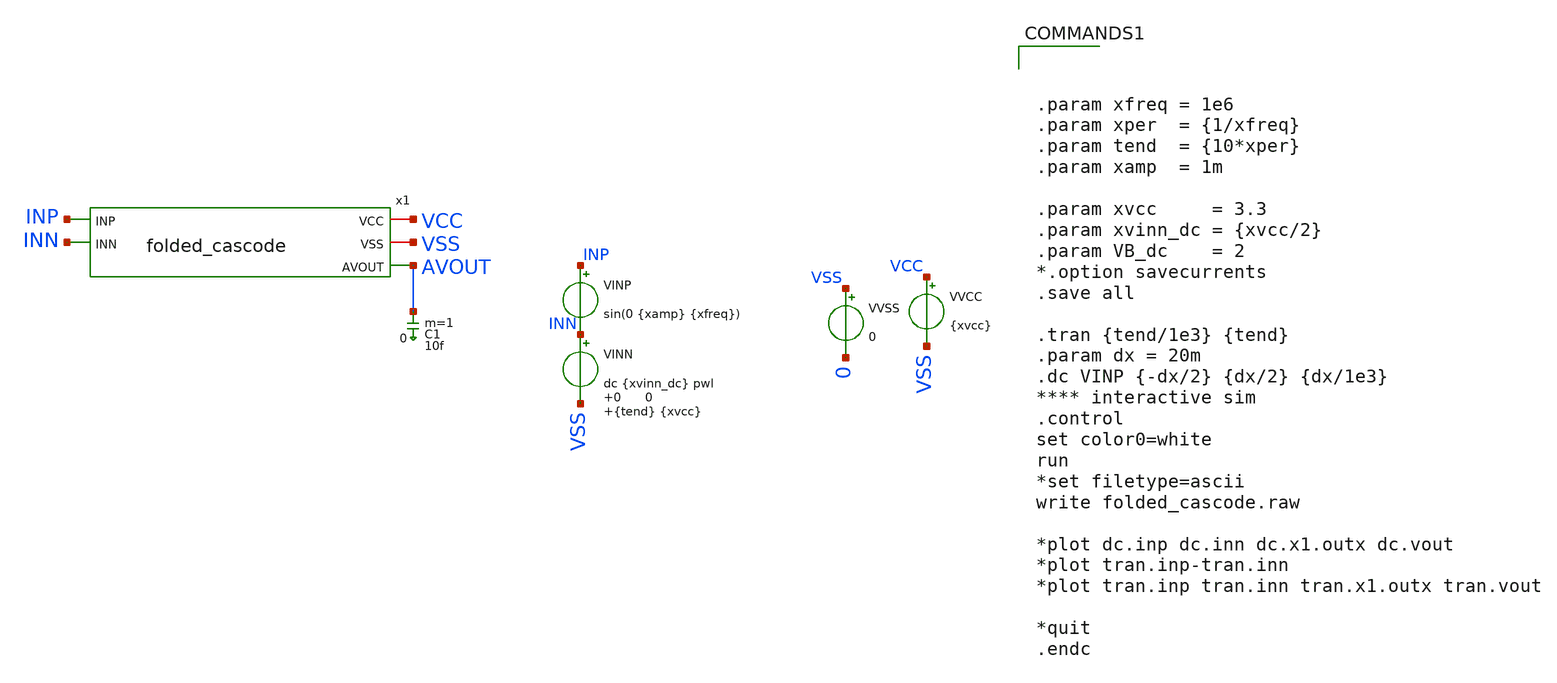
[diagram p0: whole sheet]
** sch_path: folded_cascode/LUIS/folded_cascode_tb.sch

.param mc_mm_switch=0
.lib $::SKYWATER_MODELS/sky130.lib.spice.tt.red tt
.include $::SKYWATER_STDCELLS/sky130_fd_sc_hd.spice

**.subckt folded_cascode_tb
VINP INP INN sin(0 {xamp} {xfreq})
VVSS VSS 0 0
VVCC VCC VSS {xvcc}
VINN INN VSS dc {xvinn_dc} pwl 0 0 {tend} {xvcc}

x1 VCC VSS AVOUT INP INN folded_cascode
C1 AVOUT 0 10f m=1
**** begin user architecture code



.param xfreq = 1e6
.param xper  = {1/xfreq}
.param tend  = {10*xper}
.param xamp  = 1m

.param xvcc     = 3.3
.param xvinn_dc = {xvcc/2}
.param VB_dc    = 2
*.option savecurrents
.save all

.tran {tend/1e3} {tend}
.param dx = 20m
.dc VINP {-dx/2} {dx/2} {dx/1e3}
**** interactive sim
.control
set color0=white
run
*set filetype=ascii
write folded_cascode.raw

*plot dc.inp dc.inn dc.x1.outx dc.vout
*plot tran.inp-tran.inn
*plot tran.inp tran.inn tran.x1.outx tran.vout

*quit
.endc


**** end user architecture code
**.ends

* expanding   symbol:  folded_cascode.sym # of pins=5
** sym_path: folded_cascode/LUIS/folded_cascode.sym
** sch_path: folded_cascode/LUIS/folded_cascode.sch
.subckt folded_cascode VCC VSS AVOUT INP INN
*.iopin VCC
*.iopin VSS
*.ipin INN
*.ipin INP
*.opin AVOUT
XM41 VCC VCC net1 VSS sky130_fd_pr__nfet_g5v0d10v5 L=0.5 W=1 nf=1 ad='int((nf+1)/2) * W/nf * 0.29' as='int((nf+2)/2) * W/nf * 0.29'
+ pd='2*int((nf+1)/2) * (W/nf + 0.29)' ps='2*int((nf+2)/2) * (W/nf + 0.29)' nrd='0.29 / W' nrs='0.29 / W'
+ sa=0 sb=0 sd=0 mult=1 m=1
XM42 net1 net1 bn0 VSS sky130_fd_pr__nfet_g5v0d10v5 L=0.5 W=1 nf=1 ad='int((nf+1)/2) * W/nf * 0.29' as='int((nf+2)/2) * W/nf * 0.29'
+ pd='2*int((nf+1)/2) * (W/nf + 0.29)' ps='2*int((nf+2)/2) * (W/nf + 0.29)' nrd='0.29 / W' nrs='0.29 / W'
+ sa=0 sb=0 sd=0 mult=1 m=1
XM8 bp1 bn0 VSS VSS sky130_fd_pr__nfet_g5v0d10v5 L=0.5 W=1 nf=1 ad='int((nf+1)/2) * W/nf * 0.29' as='int((nf+2)/2) * W/nf * 0.29'
+ pd='2*int((nf+1)/2) * (W/nf + 0.29)' ps='2*int((nf+2)/2) * (W/nf + 0.29)' nrd='0.29 / W' nrs='0.29 / W'
+ sa=0 sb=0 sd=0 mult=1 m=1
XM38 net2 bp1 VCC VCC sky130_fd_pr__pfet_g5v0d10v5 L=0.5 W=3 nf=1 ad='int((nf+1)/2) * W/nf * 0.29' as='int((nf+2)/2) * W/nf * 0.29'
+ pd='2*int((nf+1)/2) * (W/nf + 0.29)' ps='2*int((nf+2)/2) * (W/nf + 0.29)' nrd='0.29 / W' nrs='0.29 / W'
+ sa=0 sb=0 sd=0 mult=1 m=1
XM40 bp1 bp2 net2 VCC sky130_fd_pr__pfet_g5v0d10v5 L=0.5 W=3 nf=1 ad='int((nf+1)/2) * W/nf * 0.29' as='int((nf+2)/2) * W/nf * 0.29'
+ pd='2*int((nf+1)/2) * (W/nf + 0.29)' ps='2*int((nf+2)/2) * (W/nf + 0.29)' nrd='0.29 / W' nrs='0.29 / W'
+ sa=0 sb=0 sd=0 mult=4 m=4
XM43 net3 bp1 VCC VCC sky130_fd_pr__pfet_g5v0d10v5 L=0.5 W=3 nf=1 ad='int((nf+1)/2) * W/nf * 0.29' as='int((nf+2)/2) * W/nf * 0.29'
+ pd='2*int((nf+1)/2) * (W/nf + 0.29)' ps='2*int((nf+2)/2) * (W/nf + 0.29)' nrd='0.29 / W' nrs='0.29 / W'
+ sa=0 sb=0 sd=0 mult=1 m=1
XM44 bn1 bp2 net3 VCC sky130_fd_pr__pfet_g5v0d10v5 L=0.5 W=3 nf=1 ad='int((nf+1)/2) * W/nf * 0.29' as='int((nf+2)/2) * W/nf * 0.29'
+ pd='2*int((nf+1)/2) * (W/nf + 0.29)' ps='2*int((nf+2)/2) * (W/nf + 0.29)' nrd='0.29 / W' nrs='0.29 / W'
+ sa=0 sb=0 sd=0 mult=4 m=4
XM49 bn1 bn2 net4 VSS sky130_fd_pr__nfet_g5v0d10v5 L=0.5 W=1 nf=1 ad='int((nf+1)/2) * W/nf * 0.29' as='int((nf+2)/2) * W/nf * 0.29'
+ pd='2*int((nf+1)/2) * (W/nf + 0.29)' ps='2*int((nf+2)/2) * (W/nf + 0.29)' nrd='0.29 / W' nrs='0.29 / W'
+ sa=0 sb=0 sd=0 mult=4 m=4
XM51 net4 bn1 VSS VSS sky130_fd_pr__nfet_g5v0d10v5 L=0.5 W=1 nf=1 ad='int((nf+1)/2) * W/nf * 0.29' as='int((nf+2)/2) * W/nf * 0.29'
+ pd='2*int((nf+1)/2) * (W/nf + 0.29)' ps='2*int((nf+2)/2) * (W/nf + 0.29)' nrd='0.29 / W' nrs='0.29 / W'
+ sa=0 sb=0 sd=0 mult=1 m=1
XM19 bp2 bn0 VSS VSS sky130_fd_pr__nfet_g5v0d10v5 L=0.5 W=1 nf=1 ad='int((nf+1)/2) * W/nf * 0.29' as='int((nf+2)/2) * W/nf * 0.29'
+ pd='2*int((nf+1)/2) * (W/nf + 0.29)' ps='2*int((nf+2)/2) * (W/nf + 0.29)' nrd='0.29 / W' nrs='0.29 / W'
+ sa=0 sb=0 sd=0 mult=4 m=4
XM37 bn2 bn2 VSS VSS sky130_fd_pr__nfet_g5v0d10v5 L=0.5 W=1 nf=1 ad='int((nf+1)/2) * W/nf * 0.29' as='int((nf+2)/2) * W/nf * 0.29'
+ pd='2*int((nf+1)/2) * (W/nf + 0.29)' ps='2*int((nf+2)/2) * (W/nf + 0.29)' nrd='0.29 / W' nrs='0.29 / W'
+ sa=0 sb=0 sd=0 mult=1 m=1
XM4 bn0 bn0 VSS VSS sky130_fd_pr__nfet_g5v0d10v5 L=0.5 W=1 nf=1 ad='int((nf+1)/2) * W/nf * 0.29' as='int((nf+2)/2) * W/nf * 0.29'
+ pd='2*int((nf+1)/2) * (W/nf + 0.29)' ps='2*int((nf+2)/2) * (W/nf + 0.29)' nrd='0.29 / W' nrs='0.29 / W'
+ sa=0 sb=0 sd=0 mult=1 m=1
XM39 bp2 bp2 VCC VCC sky130_fd_pr__pfet_g5v0d10v5 L=0.5 W=3 nf=1 ad='int((nf+1)/2) * W/nf * 0.29' as='int((nf+2)/2) * W/nf * 0.29'
+ pd='2*int((nf+1)/2) * (W/nf + 0.29)' ps='2*int((nf+2)/2) * (W/nf + 0.29)' nrd='0.29 / W' nrs='0.29 / W'
+ sa=0 sb=0 sd=0 mult=1 m=1
XM45 bn2 bp2 VCC VCC sky130_fd_pr__pfet_g5v0d10v5 L=0.5 W=3 nf=1 ad='int((nf+1)/2) * W/nf * 0.29' as='int((nf+2)/2) * W/nf * 0.29'
+ pd='2*int((nf+1)/2) * (W/nf + 0.29)' ps='2*int((nf+2)/2) * (W/nf + 0.29)' nrd='0.29 / W' nrs='0.29 / W'
+ sa=0 sb=0 sd=0 mult=1 m=1
XM25 net7 bn0 VSS VSS sky130_fd_pr__nfet_g5v0d10v5 L=0.5 W=1 nf=1 ad='int((nf+1)/2) * W/nf * 0.29' as='int((nf+2)/2) * W/nf * 0.29'
+ pd='2*int((nf+1)/2) * (W/nf + 0.29)' ps='2*int((nf+2)/2) * (W/nf + 0.29)' nrd='0.29 / W' nrs='0.29 / W'
+ sa=0 sb=0 sd=0 mult=1 m=1
XM26 bp0 bp0 VCC VCC sky130_fd_pr__pfet_g5v0d10v5 L=0.5 W=3 nf=1 ad='int((nf+1)/2) * W/nf * 0.29' as='int((nf+2)/2) * W/nf * 0.29'
+ pd='2*int((nf+1)/2) * (W/nf + 0.29)' ps='2*int((nf+2)/2) * (W/nf + 0.29)' nrd='0.29 / W' nrs='0.29 / W'
+ sa=0 sb=0 sd=0 mult=1 m=1
XM46 net5 bn0 VSS VSS sky130_fd_pr__nfet_g5v0d10v5 L=0.5 W=1 nf=1 ad='int((nf+1)/2) * W/nf * 0.29' as='int((nf+2)/2) * W/nf * 0.29'
+ pd='2*int((nf+1)/2) * (W/nf + 0.29)' ps='2*int((nf+2)/2) * (W/nf + 0.29)' nrd='0.29 / W' nrs='0.29 / W'
+ sa=0 sb=0 sd=0 mult=2 m=2
XM47 net6 bp0 VCC VCC sky130_fd_pr__pfet_g5v0d10v5 L=0.5 W=3 nf=1 ad='int((nf+1)/2) * W/nf * 0.29' as='int((nf+2)/2) * W/nf * 0.29'
+ pd='2*int((nf+1)/2) * (W/nf + 0.29)' ps='2*int((nf+2)/2) * (W/nf + 0.29)' nrd='0.29 / W' nrs='0.29 / W'
+ sa=0 sb=0 sd=0 mult=2 m=2
XM48 yn_p INP net5 VSS sky130_fd_pr__nfet_g5v0d10v5 L=0.5 W=1 nf=1 ad='int((nf+1)/2) * W/nf * 0.29' as='int((nf+2)/2) * W/nf * 0.29'
+ pd='2*int((nf+1)/2) * (W/nf + 0.29)' ps='2*int((nf+2)/2) * (W/nf + 0.29)' nrd='0.29 / W' nrs='0.29 / W'
+ sa=0 sb=0 sd=0 mult=4 m=4
XM50 yn_n INN net5 VSS sky130_fd_pr__nfet_g5v0d10v5 L=0.5 W=1 nf=1 ad='int((nf+1)/2) * W/nf * 0.29' as='int((nf+2)/2) * W/nf * 0.29'
+ pd='2*int((nf+1)/2) * (W/nf + 0.29)' ps='2*int((nf+2)/2) * (W/nf + 0.29)' nrd='0.29 / W' nrs='0.29 / W'
+ sa=0 sb=0 sd=0 mult=4 m=4
XM52 yp_p INP net6 VCC sky130_fd_pr__pfet_g5v0d10v5 L=0.5 W=3 nf=1 ad='int((nf+1)/2) * W/nf * 0.29' as='int((nf+2)/2) * W/nf * 0.29'
+ pd='2*int((nf+1)/2) * (W/nf + 0.29)' ps='2*int((nf+2)/2) * (W/nf + 0.29)' nrd='0.29 / W' nrs='0.29 / W'
+ sa=0 sb=0 sd=0 mult=5 m=5
XM53 yp_n INN net6 VCC sky130_fd_pr__pfet_g5v0d10v5 L=0.5 W=3 nf=1 ad='int((nf+1)/2) * W/nf * 0.29' as='int((nf+2)/2) * W/nf * 0.29'
+ pd='2*int((nf+1)/2) * (W/nf + 0.29)' ps='2*int((nf+2)/2) * (W/nf + 0.29)' nrd='0.29 / W' nrs='0.29 / W'
+ sa=0 sb=0 sd=0 mult=5 m=5
XM54 outx bn2 yp_p VSS sky130_fd_pr__nfet_g5v0d10v5 L=0.5 W=1 nf=1 ad='int((nf+1)/2) * W/nf * 0.29' as='int((nf+2)/2) * W/nf * 0.29'
+ pd='2*int((nf+1)/2) * (W/nf + 0.29)' ps='2*int((nf+2)/2) * (W/nf + 0.29)' nrd='0.29 / W' nrs='0.29 / W'
+ sa=0 sb=0 sd=0 mult=8 m=8
XM55 yp_p zn VSS VSS sky130_fd_pr__nfet_g5v0d10v5 L=0.5 W=1 nf=1 ad='int((nf+1)/2) * W/nf * 0.29' as='int((nf+2)/2) * W/nf * 0.29'
+ pd='2*int((nf+1)/2) * (W/nf + 0.29)' ps='2*int((nf+2)/2) * (W/nf + 0.29)' nrd='0.29 / W' nrs='0.29 / W'
+ sa=0 sb=0 sd=0 mult=2 m=2
XM56 zn bn2 yp_n VSS sky130_fd_pr__nfet_g5v0d10v5 L=0.5 W=1 nf=1 ad='int((nf+1)/2) * W/nf * 0.29' as='int((nf+2)/2) * W/nf * 0.29'
+ pd='2*int((nf+1)/2) * (W/nf + 0.29)' ps='2*int((nf+2)/2) * (W/nf + 0.29)' nrd='0.29 / W' nrs='0.29 / W'
+ sa=0 sb=0 sd=0 mult=8 m=8
XM57 yp_n zn VSS VSS sky130_fd_pr__nfet_g5v0d10v5 L=0.5 W=1 nf=1 ad='int((nf+1)/2) * W/nf * 0.29' as='int((nf+2)/2) * W/nf * 0.29'
+ pd='2*int((nf+1)/2) * (W/nf + 0.29)' ps='2*int((nf+2)/2) * (W/nf + 0.29)' nrd='0.29 / W' nrs='0.29 / W'
+ sa=0 sb=0 sd=0 mult=2 m=2
XM58 zn bp0 VCC VCC sky130_fd_pr__pfet_g5v0d10v5 L=0.5 W=3 nf=1 ad='int((nf+1)/2) * W/nf * 0.29' as='int((nf+2)/2) * W/nf * 0.29'
+ pd='2*int((nf+1)/2) * (W/nf + 0.29)' ps='2*int((nf+2)/2) * (W/nf + 0.29)' nrd='0.29 / W' nrs='0.29 / W'
+ sa=0 sb=0 sd=0 mult=1 m=1
XM59 yn_n zp VCC VCC sky130_fd_pr__pfet_g5v0d10v5 L=0.5 W=3 nf=1 ad='int((nf+1)/2) * W/nf * 0.29' as='int((nf+2)/2) * W/nf * 0.29'
+ pd='2*int((nf+1)/2) * (W/nf + 0.29)' ps='2*int((nf+2)/2) * (W/nf + 0.29)' nrd='0.29 / W' nrs='0.29 / W'
+ sa=0 sb=0 sd=0 mult=2 m=2
XM60 zp bp2 yn_n VCC sky130_fd_pr__pfet_g5v0d10v5 L=0.5 W=3 nf=1 ad='int((nf+1)/2) * W/nf * 0.29' as='int((nf+2)/2) * W/nf * 0.29'
+ pd='2*int((nf+1)/2) * (W/nf + 0.29)' ps='2*int((nf+2)/2) * (W/nf + 0.29)' nrd='0.29 / W' nrs='0.29 / W'
+ sa=0 sb=0 sd=0 mult=8 m=8
XM61 yn_p zp VCC VCC sky130_fd_pr__pfet_g5v0d10v5 L=0.5 W=3 nf=1 ad='int((nf+1)/2) * W/nf * 0.29' as='int((nf+2)/2) * W/nf * 0.29'
+ pd='2*int((nf+1)/2) * (W/nf + 0.29)' ps='2*int((nf+2)/2) * (W/nf + 0.29)' nrd='0.29 / W' nrs='0.29 / W'
+ sa=0 sb=0 sd=0 mult=2 m=2
XM62 outx bp2 yn_p VCC sky130_fd_pr__pfet_g5v0d10v5 L=0.5 W=3 nf=1 ad='int((nf+1)/2) * W/nf * 0.29' as='int((nf+2)/2) * W/nf * 0.29'
+ pd='2*int((nf+1)/2) * (W/nf + 0.29)' ps='2*int((nf+2)/2) * (W/nf + 0.29)' nrd='0.29 / W' nrs='0.29 / W'
+ sa=0 sb=0 sd=0 mult=8 m=8
XM63 zp bn0 VSS VSS sky130_fd_pr__nfet_g5v0d10v5 L=0.5 W=1 nf=1 ad='int((nf+1)/2) * W/nf * 0.29' as='int((nf+2)/2) * W/nf * 0.29'
+ pd='2*int((nf+1)/2) * (W/nf + 0.29)' ps='2*int((nf+2)/2) * (W/nf + 0.29)' nrd='0.29 / W' nrs='0.29 / W'
+ sa=0 sb=0 sd=0 mult=1 m=1
XM11 net7 net7 bp0 VCC sky130_fd_pr__pfet_g5v0d10v5 L=0.5 W=3 nf=1 ad='int((nf+1)/2) * W/nf * 0.29' as='int((nf+2)/2) * W/nf * 0.29'
+ pd='2*int((nf+1)/2) * (W/nf + 0.29)' ps='2*int((nf+2)/2) * (W/nf + 0.29)' nrd='0.29 / W' nrs='0.29 / W'
+ sa=0 sb=0 sd=0 mult=1 m=1
XM15 AVOUT outx VSS VSS sky130_fd_pr__nfet_g5v0d10v5 L=4 W=2 nf=1 ad='int((nf+1)/2) * W/nf * 0.29' as='int((nf+2)/2) * W/nf * 0.29'
+ pd='2*int((nf+1)/2) * (W/nf + 0.29)' ps='2*int((nf+2)/2) * (W/nf + 0.29)' nrd='0.29 / W' nrs='0.29 / W'
+ sa=0 sb=0 sd=0 mult=1 m=1
XM14 AVOUT bp2 VCC VCC sky130_fd_pr__pfet_g5v0d10v5 L=2 W=6 nf=1 ad='int((nf+1)/2) * W/nf * 0.29' as='int((nf+2)/2) * W/nf * 0.29'
+ pd='2*int((nf+1)/2) * (W/nf + 0.29)' ps='2*int((nf+2)/2) * (W/nf + 0.29)' nrd='0.29 / W' nrs='0.29 / W'
+ sa=0 sb=0 sd=0 mult=3 m=3
.ends

.end
